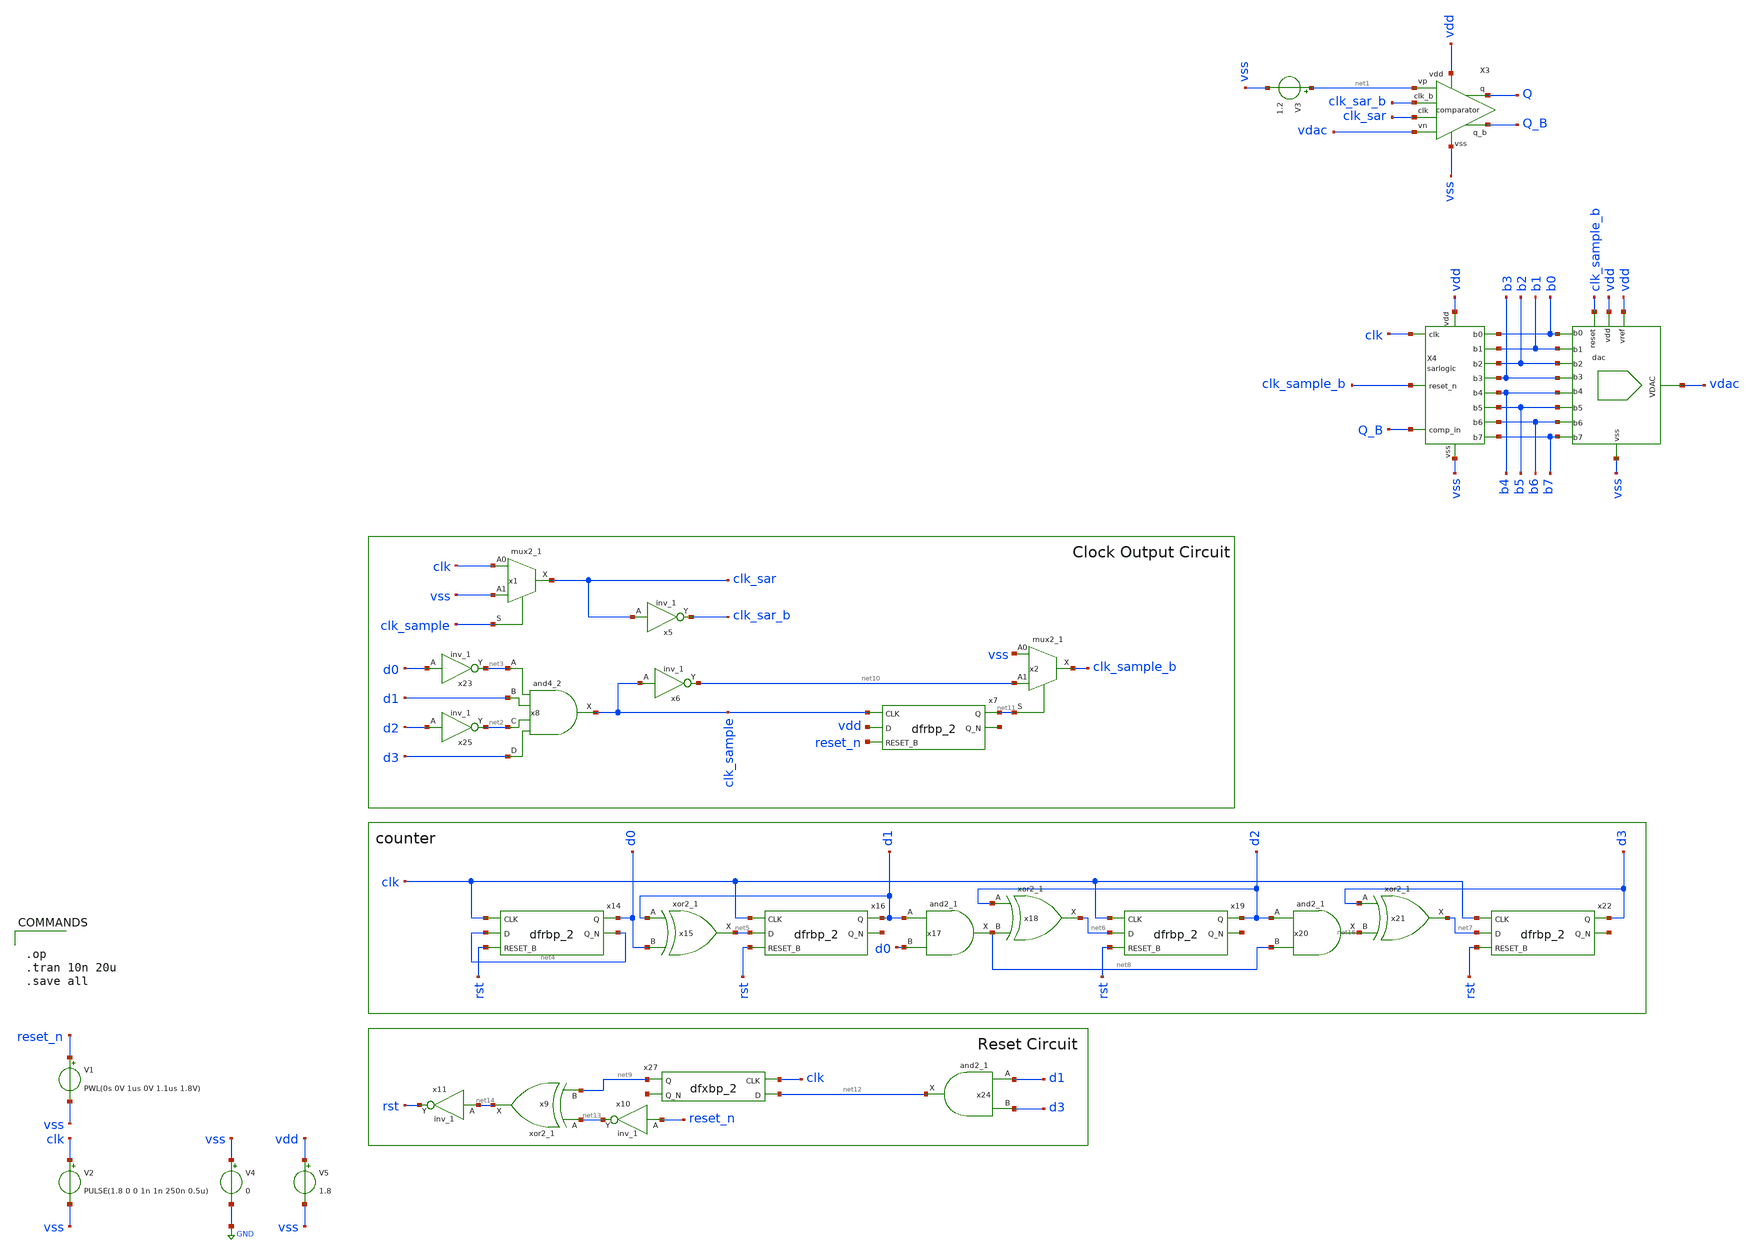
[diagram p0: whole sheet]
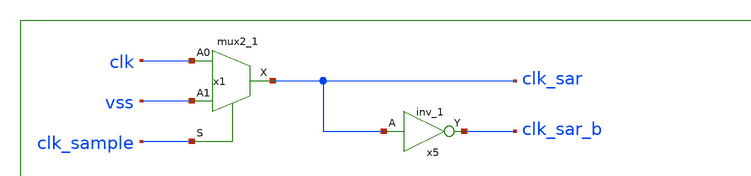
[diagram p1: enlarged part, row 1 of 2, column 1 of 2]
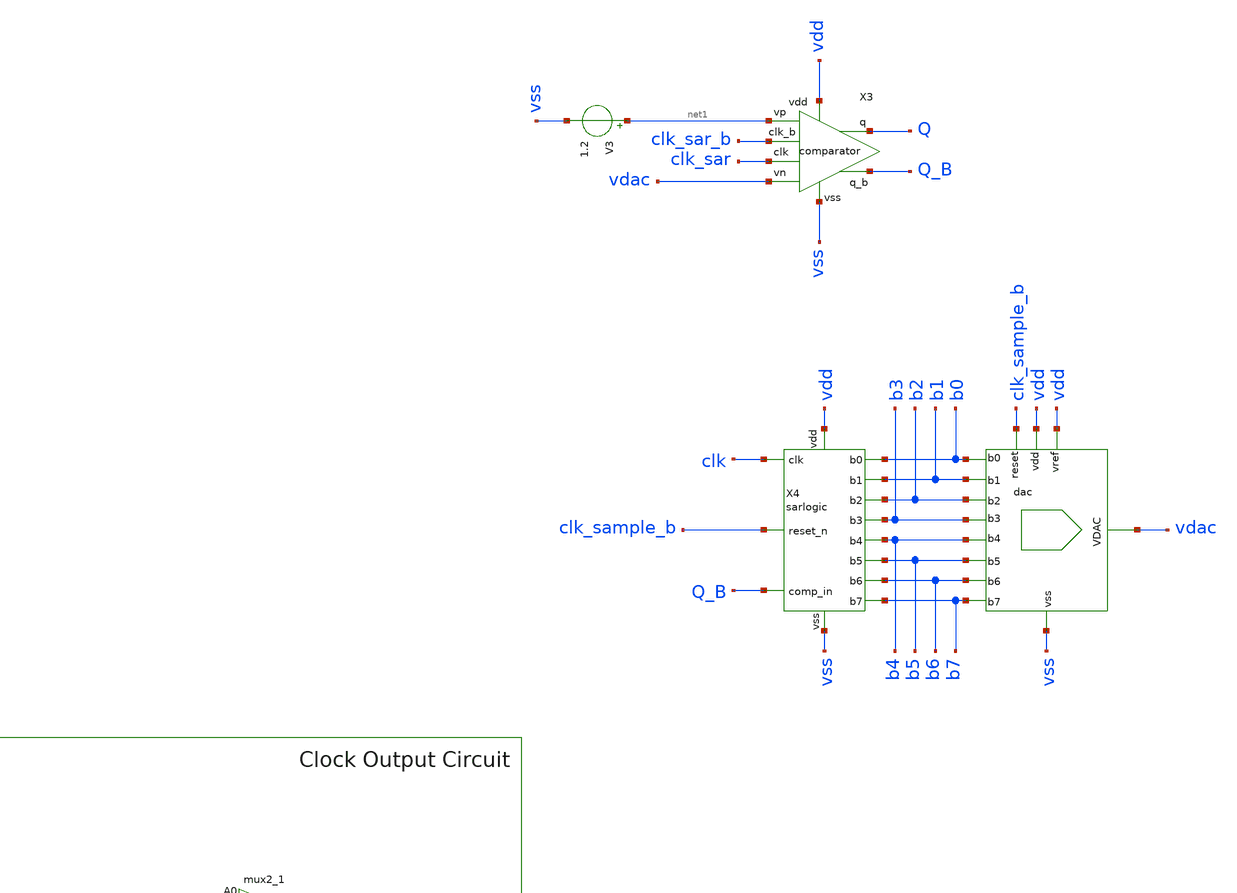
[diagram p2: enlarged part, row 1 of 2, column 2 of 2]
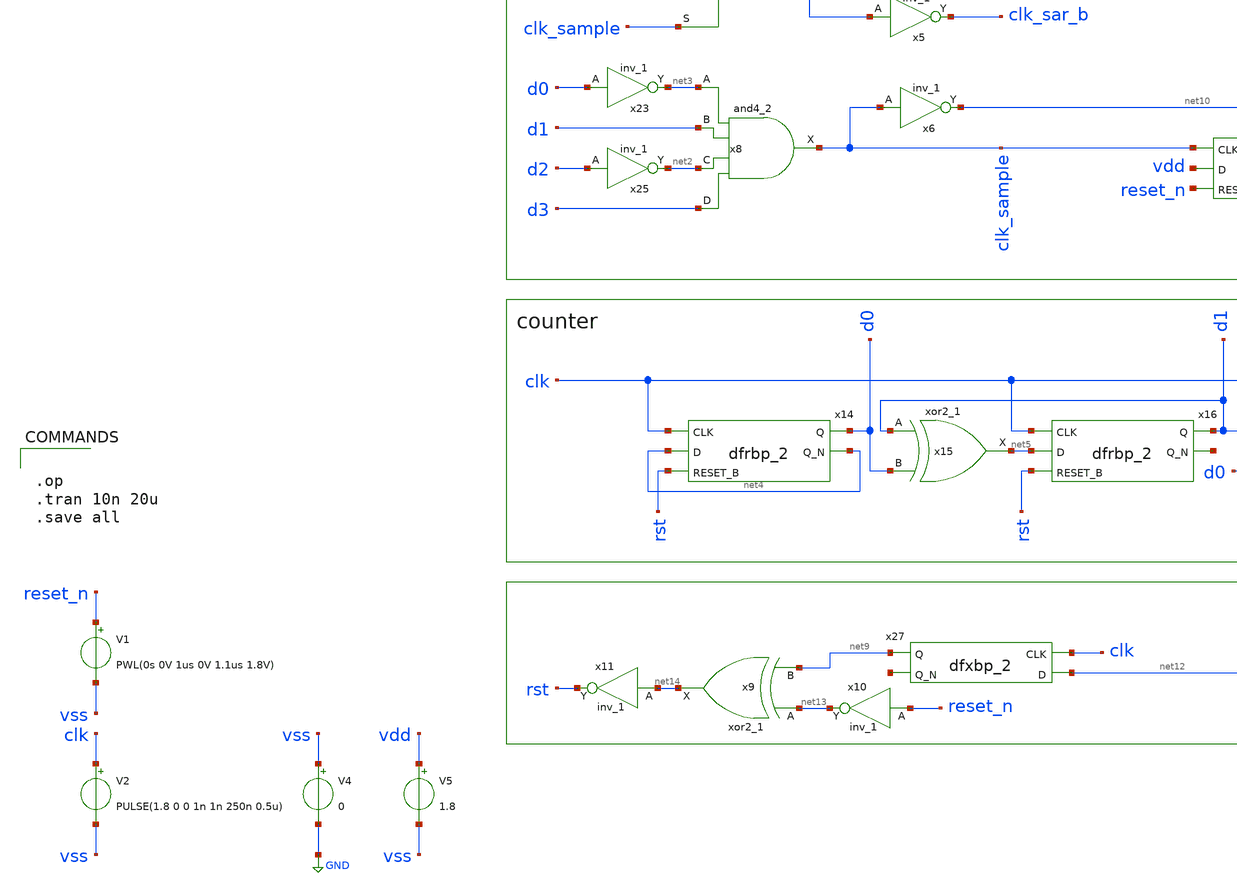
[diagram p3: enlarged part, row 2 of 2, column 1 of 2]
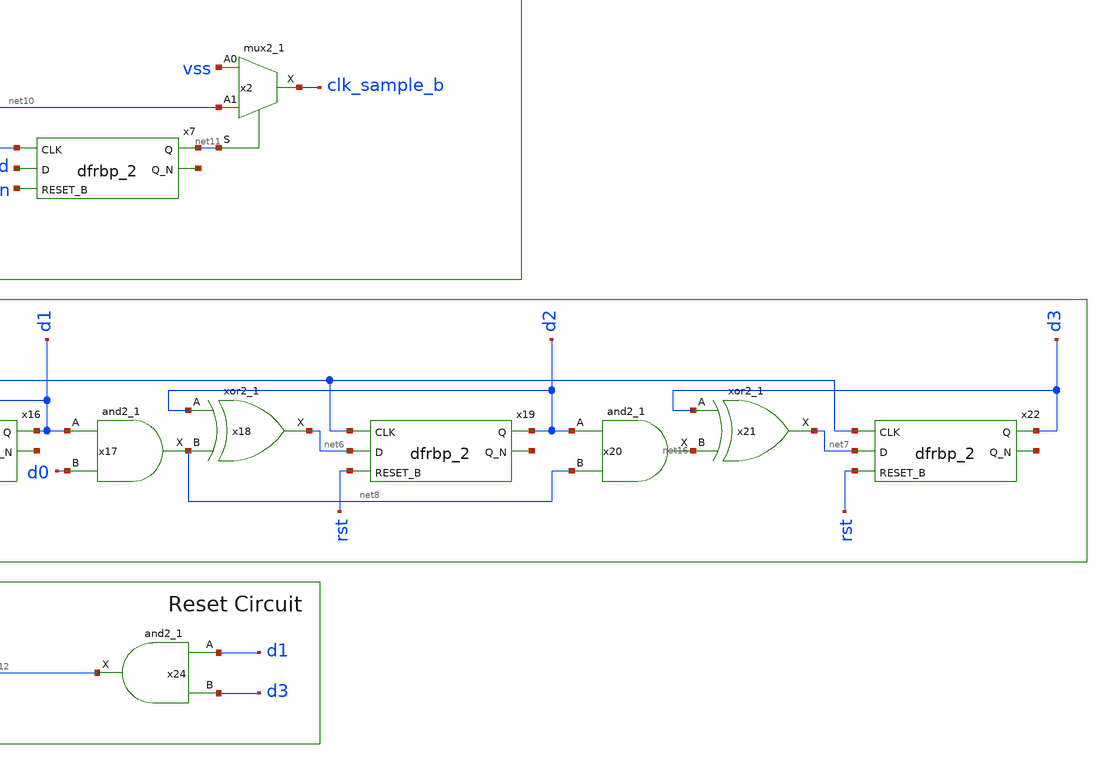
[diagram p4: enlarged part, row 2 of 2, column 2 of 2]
** sch_path: xschem/clockgen/clockgen_tb.sch
.lib $::SKYWATER_MODELS/sky130.lib.spice tt
.include $::SKYWATER_STDCELLS/sky130_fd_sc_hd.spice

**.subckt clockgen_tb
V2 clk vss PULSE(1.8 0 0 1n 1n 250n 0.5u)
X4 b0 b1 clk clk_sample_b Q_B vdd vss b2 b3 b4 b5 b6 b7 sarlogic
V1 reset_n vss PWL(0s 0V 1us 0V 1.1us 1.8V)
X1 vss vdac vdd vdd b0 b1 b2 b3 b4 b5 b6 b7 clk_sample_b dac
X3 net1 vdac vss Q_B Q vdd clk_sar clk_sar_b comparator
V3 net1 vss 1.2
V4 vss GND 0
V5 vdd vss 1.8
x1 clk vss clk_sample vss vss vdd vdd clk_sar sky130_fd_sc_hd__mux2_1
x8 net3 d1 net2 d3 vss vss vdd vdd clk_sample sky130_fd_sc_hd__and4_2
x14 clk net4 rst vss vss vdd vdd d0 net4 sky130_fd_sc_hd__dfrbp_2
x15 d1 d0 vss vss vdd vdd net5 sky130_fd_sc_hd__xor2_1
x16 clk net5 rst vss vss vdd vdd d1 net15 sky130_fd_sc_hd__dfrbp_2
x17 d1 d0 vss vss vdd vdd net8 sky130_fd_sc_hd__and2_1
x18 d2 net8 vss vss vdd vdd net6 sky130_fd_sc_hd__xor2_1
x20 d2 net8 vss vss vdd vdd net16 sky130_fd_sc_hd__and2_1
x21 d3 net16 vss vss vdd vdd net7 sky130_fd_sc_hd__xor2_1
x19 clk net6 rst vss vss vdd vdd d2 net17 sky130_fd_sc_hd__dfrbp_2
x22 clk net7 rst vss vss vdd vdd d3 net18 sky130_fd_sc_hd__dfrbp_2
x23 d0 vss vss vdd vdd net3 sky130_fd_sc_hd__inv_1
x25 d2 vss vss vdd vdd net2 sky130_fd_sc_hd__inv_1
x24 d1 d3 vss vss vdd vdd net12 sky130_fd_sc_hd__and2_1
x27 clk net12 vss vss vdd vdd net9 net19 sky130_fd_sc_hd__dfxbp_2
x5 clk_sar vss vss vdd vdd clk_sar_b sky130_fd_sc_hd__inv_1
x6 clk_sample vss vss vdd vdd net10 sky130_fd_sc_hd__inv_1
x7 clk_sample vdd reset_n vss vss vdd vdd net11 net20 sky130_fd_sc_hd__dfrbp_2
x9 net13 net9 vss vss vdd vdd net14 sky130_fd_sc_hd__xor2_1
x10 reset_n vss vss vdd vdd net13 sky130_fd_sc_hd__inv_1
x11 net14 vss vss vdd vdd rst sky130_fd_sc_hd__inv_1
x2 vss net10 net11 vss vss vdd vdd clk_sample_b sky130_fd_sc_hd__mux2_1
**** begin user architecture code


.op
.tran 10n 20u
.save all


**** end user architecture code
**.ends

* expanding   symbol:  xschem/sar_logic/sarlogic.sym # of pins=13
** sym_path: xschem/sar_logic/sarlogic.sym
** sch_path: xschem/sar_logic/sarlogic.sch
.subckt sarlogic b0 b1 clk reset_n comp_in vdd vss b2 b3 b4 b5 b6 b7
*.iopin vdd
*.iopin clk
*.iopin b7
*.iopin b6
*.iopin b5
*.iopin b4
*.iopin b3
*.iopin b2
*.iopin b1
*.iopin b0
*.iopin comp_in
*.iopin vss
*.iopin reset_n
x35 clk df7 net1 vdd vss vss vdd vdd df6 df6_b sky130_fd_sc_hd__dfbbp_1
x36 clk df6 net1 vdd vss vss vdd vdd df5 df5_b sky130_fd_sc_hd__dfbbp_1
x37 clk df5 net1 vdd vss vss vdd vdd df4 df4_b sky130_fd_sc_hd__dfbbp_1
x38 clk df4 net1 vdd vss vss vdd vdd df3 df3_b sky130_fd_sc_hd__dfbbp_1
x39 clk df3 net1 vdd vss vss vdd vdd df2 df2_b sky130_fd_sc_hd__dfbbp_1
x40 clk df2 net1 vdd vss vss vdd vdd df1 df1_b sky130_fd_sc_hd__dfbbp_1
x41 clk df1 net1 vdd vss vss vdd vdd df0 df0_b sky130_fd_sc_hd__dfbbp_1
x42 clk df0 net1 vdd vss vss vdd vdd df00 df00_b sky130_fd_sc_hd__dfbbp_1
x43 b5 net3 net1 df6_b vss vss vdd vdd b6 net4 sky130_fd_sc_hd__dfbbp_1
x44 b4 net3 net1 df5_b vss vss vdd vdd b5 net5 sky130_fd_sc_hd__dfbbp_1
x2 b3 net3 net1 df4_b vss vss vdd vdd b4 net6 sky130_fd_sc_hd__dfbbp_1
x46 b2 net3 net1 df3_b vss vss vdd vdd b3 net7 sky130_fd_sc_hd__dfbbp_1
x47 b1 net3 net1 df2_b vss vss vdd vdd b2 net8 sky130_fd_sc_hd__dfbbp_1
x48 b0 net3 net1 df1_b vss vss vdd vdd b1 net9 sky130_fd_sc_hd__dfbbp_1
x49 net2 net3 net1 df0_b vss vss vdd vdd b0 net10 sky130_fd_sc_hd__dfbbp_1
x50 vss vss net1 df00_b vss vss vdd vdd net2 net11 sky130_fd_sc_hd__dfbbp_1
x51 clk vss vdd net1 vss vss vdd vdd df7 df7_b sky130_fd_sc_hd__dfbbp_1
x52 b6 net3 net1 df7_b vss vss vdd vdd b7 net12 sky130_fd_sc_hd__dfbbp_1
x53 clk reset_n vss vss vdd vdd net1 net13 sky130_fd_sc_hd__dfxbp_2
x9 comp_in vss vss vdd vdd net3 sky130_fd_sc_hd__inv_1
.ends


* expanding   symbol:  xschem/dac/dac.sym # of pins=13
** sym_path: xschem/dac/dac.sym
** sch_path: xschem/dac/dac.sch
.subckt dac vss vdac vdd vref s0 s1 s2 s3 s4 s5 s6 s7 reset
*.ipin s7
*.ipin s6
*.ipin s5
*.ipin s4
*.ipin s3
*.ipin s2
*.ipin s1
*.ipin s0
*.iopin vdd
*.iopin vss
*.iopin vref
*.opin vdac
*.ipin reset
XC2 net1 net2 sky130_fd_pr__cap_mim_m3_1 W=w L=l MF=8 m=8
X2 net2 vref vss vdd net14 vss dac_sw
XC1 net1 net3 sky130_fd_pr__cap_mim_m3_1 W=w L=l MF=4 m=4
X3 net3 vref vss vdd net15 vss dac_sw
X4 net4 vref vss vdd net16 vss dac_sw
X5 net5 vref vss vdd net17 vss dac_sw
XC3 net1 net4 sky130_fd_pr__cap_mim_m3_1 W=w L=l MF=2 m=2
XC4 net1 net5 sky130_fd_pr__cap_mim_m3_1 W=w L=l MF=1 m=1
XC5 vss net1 sky130_fd_pr__cap_mim_m3_1 W=w L=l MF=1 m=1
XC6 vdac net6 sky130_fd_pr__cap_mim_m3_1 W=w L=l MF=1 m=1
X1 net6 vref vss vdd net13 vss dac_sw
XC7 vdac net7 sky130_fd_pr__cap_mim_m3_1 W=w L=l MF=2 m=2
X6 net7 vref vss vdd net12 vss dac_sw
XC8 vdac net8 sky130_fd_pr__cap_mim_m3_1 W=w L=l MF=4 m=4
X7 net8 vref vss vdd net11 vss dac_sw
XC9 vdac net9 sky130_fd_pr__cap_mim_m3_1 W=w L=l MF=8 m=8
X8 net9 vref vss vdd net10 vss dac_sw
x9 vss s7 reset vss vss vdd vdd net10 sky130_fd_sc_hd__mux2_1
x10 vss s6 reset vss vss vdd vdd net11 sky130_fd_sc_hd__mux2_1
x11 vss s5 reset vss vss vdd vdd net12 sky130_fd_sc_hd__mux2_1
x12 vss s4 reset vss vss vdd vdd net13 sky130_fd_sc_hd__mux2_1
x13 vss s3 reset vss vss vdd vdd net14 sky130_fd_sc_hd__mux2_1
x14 vss s2 reset vss vss vdd vdd net15 sky130_fd_sc_hd__mux2_1
x15 vss s1 reset vss vss vdd vdd net16 sky130_fd_sc_hd__mux2_1
x16 vss s0 reset vss vss vdd vdd net17 sky130_fd_sc_hd__mux2_1
XM1 vdac net18 vss vss sky130_fd_pr__nfet_01v8 L=0.15 W=1 nf=1 ad='int((nf+1)/2) * W/nf * 0.29' as='int((nf+2)/2) * W/nf * 0.29'
+ pd='2*int((nf+1)/2) * (W/nf + 0.29)' ps='2*int((nf+2)/2) * (W/nf + 0.29)' nrd='0.29 / W' nrs='0.29 / W'
+ sa=0 sb=0 sd=0 mult=1 m=1
x17 reset vss vss vdd vdd net18 sky130_fd_sc_hd__inv_1
XM2 net1 net19 vss vss sky130_fd_pr__nfet_01v8 L=0.15 W=1 nf=1 ad='int((nf+1)/2) * W/nf * 0.29' as='int((nf+2)/2) * W/nf * 0.29'
+ pd='2*int((nf+1)/2) * (W/nf + 0.29)' ps='2*int((nf+2)/2) * (W/nf + 0.29)' nrd='0.29 / W' nrs='0.29 / W'
+ sa=0 sb=0 sd=0 mult=1 m=1
x18 reset vss vss vdd vdd net19 sky130_fd_sc_hd__inv_1
XC10 net1 vdac sky130_fd_pr__cap_mim_m3_1 W=w L=l MF=8/7 m=8/7
.ends


* expanding   symbol:  xschem/comparator/comparator.sym # of pins=8
** sym_path: xschem/comparator/comparator.sym
** sch_path: xschem/comparator/comparator.sch
.subckt comparator vp vn vss q_b q vdd clk clk_b
*.ipin vp
*.ipin vn
*.iopin vdd
*.ipin clk
*.iopin vss
*.opin q
*.opin q_b
*.ipin clk_b
X4 vp vn vss net2 net1 vdd clk preamp
X6 net1 net2 vss q_b q vdd clk_b strongarm
.ends


* expanding   symbol:  xschem/dac/dac_sw.sym # of pins=6
** sym_path: xschem/dac/dac_sw.sym
** sch_path: xschem/dac/dac_sw.sch
.subckt dac_sw c b vss vdd clk a
*.iopin vdd
*.iopin vss
*.ipin clk
*.iopin c
*.iopin a
*.iopin b
XM2 c clk b vss sky130_fd_pr__nfet_01v8 L=0.15 W=5 nf=1 ad='int((nf+1)/2) * W/nf * 0.29' as='int((nf+2)/2) * W/nf * 0.29'
+ pd='2*int((nf+1)/2) * (W/nf + 0.29)' ps='2*int((nf+2)/2) * (W/nf + 0.29)' nrd='0.29 / W' nrs='0.29 / W'
+ sa=0 sb=0 sd=0 mult=1 m=1
XM5 b net1 c vdd sky130_fd_pr__pfet_01v8 L=0.15 W=10 nf=1 ad='int((nf+1)/2) * W/nf * 0.29' as='int((nf+2)/2) * W/nf * 0.29'
+ pd='2*int((nf+1)/2) * (W/nf + 0.29)' ps='2*int((nf+2)/2) * (W/nf + 0.29)' nrd='0.29 / W' nrs='0.29 / W'
+ sa=0 sb=0 sd=0 mult=1 m=1
XM6 c net1 a vss sky130_fd_pr__nfet_01v8 L=0.15 W=5 nf=1 ad='int((nf+1)/2) * W/nf * 0.29' as='int((nf+2)/2) * W/nf * 0.29'
+ pd='2*int((nf+1)/2) * (W/nf + 0.29)' ps='2*int((nf+2)/2) * (W/nf + 0.29)' nrd='0.29 / W' nrs='0.29 / W'
+ sa=0 sb=0 sd=0 mult=1 m=1
XM7 a clk c vdd sky130_fd_pr__pfet_01v8 L=0.15 W=10 nf=1 ad='int((nf+1)/2) * W/nf * 0.29' as='int((nf+2)/2) * W/nf * 0.29'
+ pd='2*int((nf+1)/2) * (W/nf + 0.29)' ps='2*int((nf+2)/2) * (W/nf + 0.29)' nrd='0.29 / W' nrs='0.29 / W'
+ sa=0 sb=0 sd=0 mult=1 m=1
x1 clk vss vss vdd vdd net1 sky130_fd_sc_hd__inv_1
.ends


* expanding   symbol:  xschem/comparator/preamp.sym # of pins=7
** sym_path: xschem/comparator/preamp.sym
** sch_path: xschem/comparator/preamp.sch
.subckt preamp VP VN GND VON VOP VDD CK
*.iopin VDD
*.iopin GND
*.iopin CK
*.iopin VON
*.iopin VOP
*.iopin VP
*.iopin VN
XM5 VON VP net1 GND sky130_fd_pr__nfet_01v8 L=1.5 W=2 nf=2 ad='int((2 + 1)/2) * 2 / 2 * 0.29' as='int((2 + 2)/2) * 2 / 2 * 0.29'
+ pd='2*int((2 + 1)/2) * (2 / 2 + 0.29)' ps='2*int((2 + 2)/2) * (2 / 2 + 0.29)' nrd='0.29 / 2 ' nrs='0.29 / 2 '
+ sa=0 sb=0 sd=0 mult=1 m=1
XM6 VON VON VDD VDD sky130_fd_pr__pfet_01v8 L=1.5 W=4 nf=1 ad='int((nf+1)/2) * W/nf * 0.29' as='int((nf+2)/2) * W/nf * 0.29'
+ pd='2*int((nf+1)/2) * (W/nf + 0.29)' ps='2*int((nf+2)/2) * (W/nf + 0.29)' nrd='0.29 / W' nrs='0.29 / W'
+ sa=0 sb=0 sd=0 mult=1 m=1
XM7 VOP VOP VDD VDD sky130_fd_pr__pfet_01v8 L=1.5 W=4 nf=1 ad='int((nf+1)/2) * W/nf * 0.29' as='int((nf+2)/2) * W/nf * 0.29'
+ pd='2*int((nf+1)/2) * (W/nf + 0.29)' ps='2*int((nf+2)/2) * (W/nf + 0.29)' nrd='0.29 / W' nrs='0.29 / W'
+ sa=0 sb=0 sd=0 mult=1 m=1
XM8 VOP VN net1 GND sky130_fd_pr__nfet_01v8 L=1.5 W=2 nf=2 ad='int((2 + 1)/2) * 2 / 2 * 0.29' as='int((2 + 2)/2) * 2 / 2 * 0.29'
+ pd='2*int((2 + 1)/2) * (2 / 2 + 0.29)' ps='2*int((2 + 2)/2) * (2 / 2 + 0.29)' nrd='0.29 / 2 ' nrs='0.29 / 2 '
+ sa=0 sb=0 sd=0 mult=1 m=1
XM9 net1 CK GND GND sky130_fd_pr__nfet_01v8 L=1 W=4 nf=1 ad='int((1 + 1)/2) * 4 / 1 * 0.29' as='int((1 + 2)/2) * 4 / 1 * 0.29'
+ pd='2*int((1 + 1)/2) * (4 / 1 + 0.29)' ps='2*int((1 + 2)/2) * (4 / 1 + 0.29)' nrd='0.29 / 4 ' nrs='0.29 / 4 '
+ sa=0 sb=0 sd=0 mult=1 m=1
.ends


* expanding   symbol:  xschem/comparator/strongarm.sym # of pins=7
** sym_path: xschem/comparator/strongarm.sym
** sch_path: xschem/comparator/strongarm.sch
.subckt strongarm VP VN GND VON VOP VDD CK
*.iopin GND
*.ipin VP
*.opin VOP
*.opin VON
*.ipin VN
*.iopin VDD
*.ipin CK
XM2 net2 CK GND GND sky130_fd_pr__nfet_01v8 L=0.15 W=2 nf=2 ad='int((nf+1)/2) * W/nf * 0.29' as='int((nf+2)/2) * W/nf * 0.29'
+ pd='2*int((nf+1)/2) * (W/nf + 0.29)' ps='2*int((nf+2)/2) * (W/nf + 0.29)' nrd='0.29 / W' nrs='0.29 / W'
+ sa=0 sb=0 sd=0 mult=1 m=1
XM4 VON CK VDD VDD sky130_fd_pr__pfet_01v8 L=0.15 W=1 nf=1 ad='int((nf+1)/2) * W/nf * 0.29' as='int((nf+2)/2) * W/nf * 0.29'
+ pd='2*int((nf+1)/2) * (W/nf + 0.29)' ps='2*int((nf+2)/2) * (W/nf + 0.29)' nrd='0.29 / W' nrs='0.29 / W'
+ sa=0 sb=0 sd=0 mult=1 m=1
XM5 net1 CK VDD VDD sky130_fd_pr__pfet_01v8 L=0.15 W=1 nf=1 ad='int((nf+1)/2) * W/nf * 0.29' as='int((nf+2)/2) * W/nf * 0.29'
+ pd='2*int((nf+1)/2) * (W/nf + 0.29)' ps='2*int((nf+2)/2) * (W/nf + 0.29)' nrd='0.29 / W' nrs='0.29 / W'
+ sa=0 sb=0 sd=0 mult=1 m=1
XM8 net1 VP net2 GND sky130_fd_pr__nfet_01v8 L=0.15 W=2.5 nf=4 ad='int((nf+1)/2) * W/nf * 0.29' as='int((nf+2)/2) * W/nf * 0.29'
+ pd='2*int((nf+1)/2) * (W/nf + 0.29)' ps='2*int((nf+2)/2) * (W/nf + 0.29)' nrd='0.29 / W' nrs='0.29 / W'
+ sa=0 sb=0 sd=0 mult=1 m=1
XM9 VON VOP net1 GND sky130_fd_pr__nfet_01v8 L=0.15 W=2.5 nf=4 ad='int((nf+1)/2) * W/nf * 0.29' as='int((nf+2)/2) * W/nf * 0.29'
+ pd='2*int((nf+1)/2) * (W/nf + 0.29)' ps='2*int((nf+2)/2) * (W/nf + 0.29)' nrd='0.29 / W' nrs='0.29 / W'
+ sa=0 sb=0 sd=0 mult=1 m=1
XM11 VOP CK VDD VDD sky130_fd_pr__pfet_01v8 L=0.15 W=1 nf=1 ad='int((nf+1)/2) * W/nf * 0.29' as='int((nf+2)/2) * W/nf * 0.29'
+ pd='2*int((nf+1)/2) * (W/nf + 0.29)' ps='2*int((nf+2)/2) * (W/nf + 0.29)' nrd='0.29 / W' nrs='0.29 / W'
+ sa=0 sb=0 sd=0 mult=1 m=1
XM12 net3 CK VDD VDD sky130_fd_pr__pfet_01v8 L=0.15 W=1 nf=1 ad='int((nf+1)/2) * W/nf * 0.29' as='int((nf+2)/2) * W/nf * 0.29'
+ pd='2*int((nf+1)/2) * (W/nf + 0.29)' ps='2*int((nf+2)/2) * (W/nf + 0.29)' nrd='0.29 / W' nrs='0.29 / W'
+ sa=0 sb=0 sd=0 mult=1 m=1
XM13 net3 VN net2 GND sky130_fd_pr__nfet_01v8 L=0.15 W=2.5 nf=4 ad='int((nf+1)/2) * W/nf * 0.29' as='int((nf+2)/2) * W/nf * 0.29'
+ pd='2*int((nf+1)/2) * (W/nf + 0.29)' ps='2*int((nf+2)/2) * (W/nf + 0.29)' nrd='0.29 / W' nrs='0.29 / W'
+ sa=0 sb=0 sd=0 mult=1 m=1
XM14 VOP VON net3 GND sky130_fd_pr__nfet_01v8 L=0.15 W=10 nf=1 ad='int((nf+1)/2) * W/nf * 0.29' as='int((nf+2)/2) * W/nf * 0.29'
+ pd='2*int((nf+1)/2) * (W/nf + 0.29)' ps='2*int((nf+2)/2) * (W/nf + 0.29)' nrd='0.29 / W' nrs='0.29 / W'
+ sa=0 sb=0 sd=0 mult=1 m=1
XM15 VOP VON VDD VDD sky130_fd_pr__pfet_01v8 L=0.15 W=2.5 nf=1 ad='int((nf+1)/2) * W/nf * 0.29' as='int((nf+2)/2) * W/nf * 0.29'
+ pd='2*int((nf+1)/2) * (W/nf + 0.29)' ps='2*int((nf+2)/2) * (W/nf + 0.29)' nrd='0.29 / W' nrs='0.29 / W'
+ sa=0 sb=0 sd=0 mult=1 m=1
XM10 VON VOP VDD VDD sky130_fd_pr__pfet_01v8 L=0.15 W=2.5 nf=1 ad='int((nf+1)/2) * W/nf * 0.29' as='int((nf+2)/2) * W/nf * 0.29'
+ pd='2*int((nf+1)/2) * (W/nf + 0.29)' ps='2*int((nf+2)/2) * (W/nf + 0.29)' nrd='0.29 / W' nrs='0.29 / W'
+ sa=0 sb=0 sd=0 mult=1 m=1
.ends

.GLOBAL GND
.end
